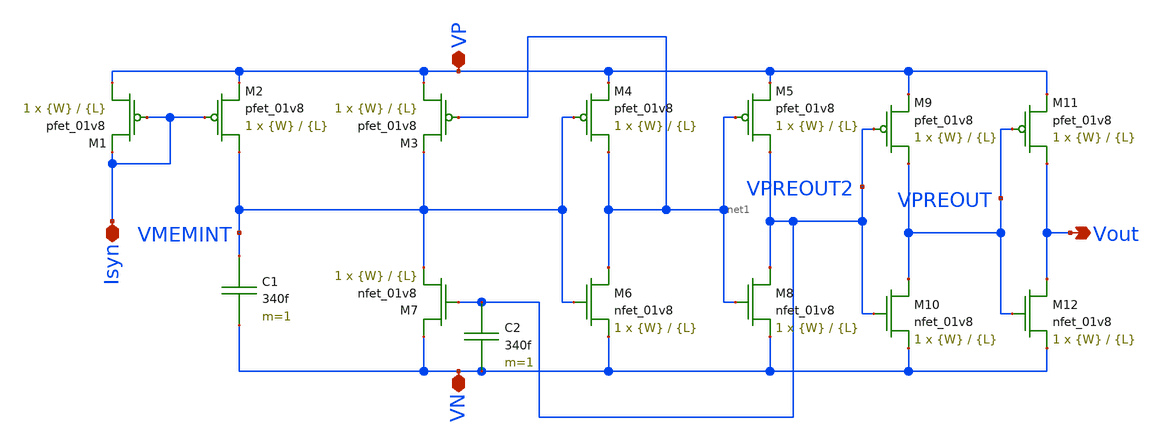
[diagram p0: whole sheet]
** sch_path: schematic/besrour_neuron.sch
**.subckt besrour_neuron VP VN Isyn Vout
*.iopin VP
*.iopin VN
*.iopin Isyn
*.opin Vout
XM1 VP Isyn Isyn VDD sky130_fd_pr__pfet_01v8 L={L} W={W} nf=1 ad='int((nf+1)/2) * W/nf * 0.29' as='int((nf+2)/2) * W/nf * 0.29'
+ pd='2*int((nf+1)/2) * (W/nf + 0.29)' ps='2*int((nf+2)/2) * (W/nf + 0.29)' nrd='0.29 / W' nrs='0.29 / W'
+ sa=0 sb=0 sd=0 mult=1 m=1
XM7 VN VPREOUT2 VMEMINT GND sky130_fd_pr__nfet_01v8 L={L} W={W} nf=1 ad='int((nf+1)/2) * W/nf * 0.29'
+ as='int((nf+2)/2) * W/nf * 0.29' pd='2*int((nf+1)/2) * (W/nf + 0.29)' ps='2*int((nf+2)/2) * (W/nf + 0.29)'
+ nrd='0.29 / W' nrs='0.29 / W' sa=0 sb=0 sd=0 mult=1 m=1
XM2 VMEMINT Isyn VP VDD sky130_fd_pr__pfet_01v8 L={L} W={W} nf=1 ad='int((nf+1)/2) * W/nf * 0.29' as='int((nf+2)/2) * W/nf * 0.29'
+ pd='2*int((nf+1)/2) * (W/nf + 0.29)' ps='2*int((nf+2)/2) * (W/nf + 0.29)' nrd='0.29 / W' nrs='0.29 / W'
+ sa=0 sb=0 sd=0 mult=1 m=1
XM3 VP net1 VMEMINT VDD sky130_fd_pr__pfet_01v8 L={L} W={W} nf=1 ad='int((nf+1)/2) * W/nf * 0.29' as='int((nf+2)/2) * W/nf * 0.29'
+ pd='2*int((nf+1)/2) * (W/nf + 0.29)' ps='2*int((nf+2)/2) * (W/nf + 0.29)' nrd='0.29 / W' nrs='0.29 / W'
+ sa=0 sb=0 sd=0 mult=1 m=1
XM4 net1 VMEMINT VP VDD sky130_fd_pr__pfet_01v8 L={L} W={W} nf=1 ad='int((nf+1)/2) * W/nf * 0.29' as='int((nf+2)/2) * W/nf * 0.29'
+ pd='2*int((nf+1)/2) * (W/nf + 0.29)' ps='2*int((nf+2)/2) * (W/nf + 0.29)' nrd='0.29 / W' nrs='0.29 / W'
+ sa=0 sb=0 sd=0 mult=1 m=1
XM5 VPREOUT2 net1 VP VDD sky130_fd_pr__pfet_01v8 L={L} W={W} nf=1 ad='int((nf+1)/2) * W/nf * 0.29' as='int((nf+2)/2) * W/nf * 0.29'
+ pd='2*int((nf+1)/2) * (W/nf + 0.29)' ps='2*int((nf+2)/2) * (W/nf + 0.29)' nrd='0.29 / W' nrs='0.29 / W'
+ sa=0 sb=0 sd=0 mult=1 m=1
XM6 net1 VMEMINT VN GND sky130_fd_pr__nfet_01v8 L={L} W={W} nf=1 ad='int((nf+1)/2) * W/nf * 0.29' as='int((nf+2)/2) * W/nf * 0.29'
+ pd='2*int((nf+1)/2) * (W/nf + 0.29)' ps='2*int((nf+2)/2) * (W/nf + 0.29)' nrd='0.29 / W' nrs='0.29 / W'
+ sa=0 sb=0 sd=0 mult=1 m=1
XM8 VPREOUT2 net1 VN GND sky130_fd_pr__nfet_01v8 L={L} W={W} nf=1 ad='int((nf+1)/2) * W/nf * 0.29' as='int((nf+2)/2) * W/nf * 0.29'
+ pd='2*int((nf+1)/2) * (W/nf + 0.29)' ps='2*int((nf+2)/2) * (W/nf + 0.29)' nrd='0.29 / W' nrs='0.29 / W'
+ sa=0 sb=0 sd=0 mult=1 m=1
C1 VMEMINT VN 340f m=1
C2 VPREOUT2 VN 340f m=1
XM9 VPREOUT VPREOUT2 VP VDD sky130_fd_pr__pfet_01v8 L={L} W={W} nf=1 ad='int((nf+1)/2) * W/nf * 0.29'
+ as='int((nf+2)/2) * W/nf * 0.29' pd='2*int((nf+1)/2) * (W/nf + 0.29)' ps='2*int((nf+2)/2) * (W/nf + 0.29)'
+ nrd='0.29 / W' nrs='0.29 / W' sa=0 sb=0 sd=0 mult=1 m=1
XM10 VPREOUT VPREOUT2 VN GND sky130_fd_pr__nfet_01v8 L={L} W={W} nf=1 ad='int((nf+1)/2) * W/nf * 0.29'
+ as='int((nf+2)/2) * W/nf * 0.29' pd='2*int((nf+1)/2) * (W/nf + 0.29)' ps='2*int((nf+2)/2) * (W/nf + 0.29)'
+ nrd='0.29 / W' nrs='0.29 / W' sa=0 sb=0 sd=0 mult=1 m=1
XM11 Vout VPREOUT VP VDD sky130_fd_pr__pfet_01v8 L={L} W={W} nf=1 ad='int((nf+1)/2) * W/nf * 0.29' as='int((nf+2)/2) * W/nf * 0.29'
+ pd='2*int((nf+1)/2) * (W/nf + 0.29)' ps='2*int((nf+2)/2) * (W/nf + 0.29)' nrd='0.29 / W' nrs='0.29 / W'
+ sa=0 sb=0 sd=0 mult=1 m=1
XM12 Vout VPREOUT VN GND sky130_fd_pr__nfet_01v8 L={L} W={W} nf=1 ad='int((nf+1)/2) * W/nf * 0.29' as='int((nf+2)/2) * W/nf * 0.29'
+ pd='2*int((nf+1)/2) * (W/nf + 0.29)' ps='2*int((nf+2)/2) * (W/nf + 0.29)' nrd='0.29 / W' nrs='0.29 / W'
+ sa=0 sb=0 sd=0 mult=1 m=1
**.ends
.end
